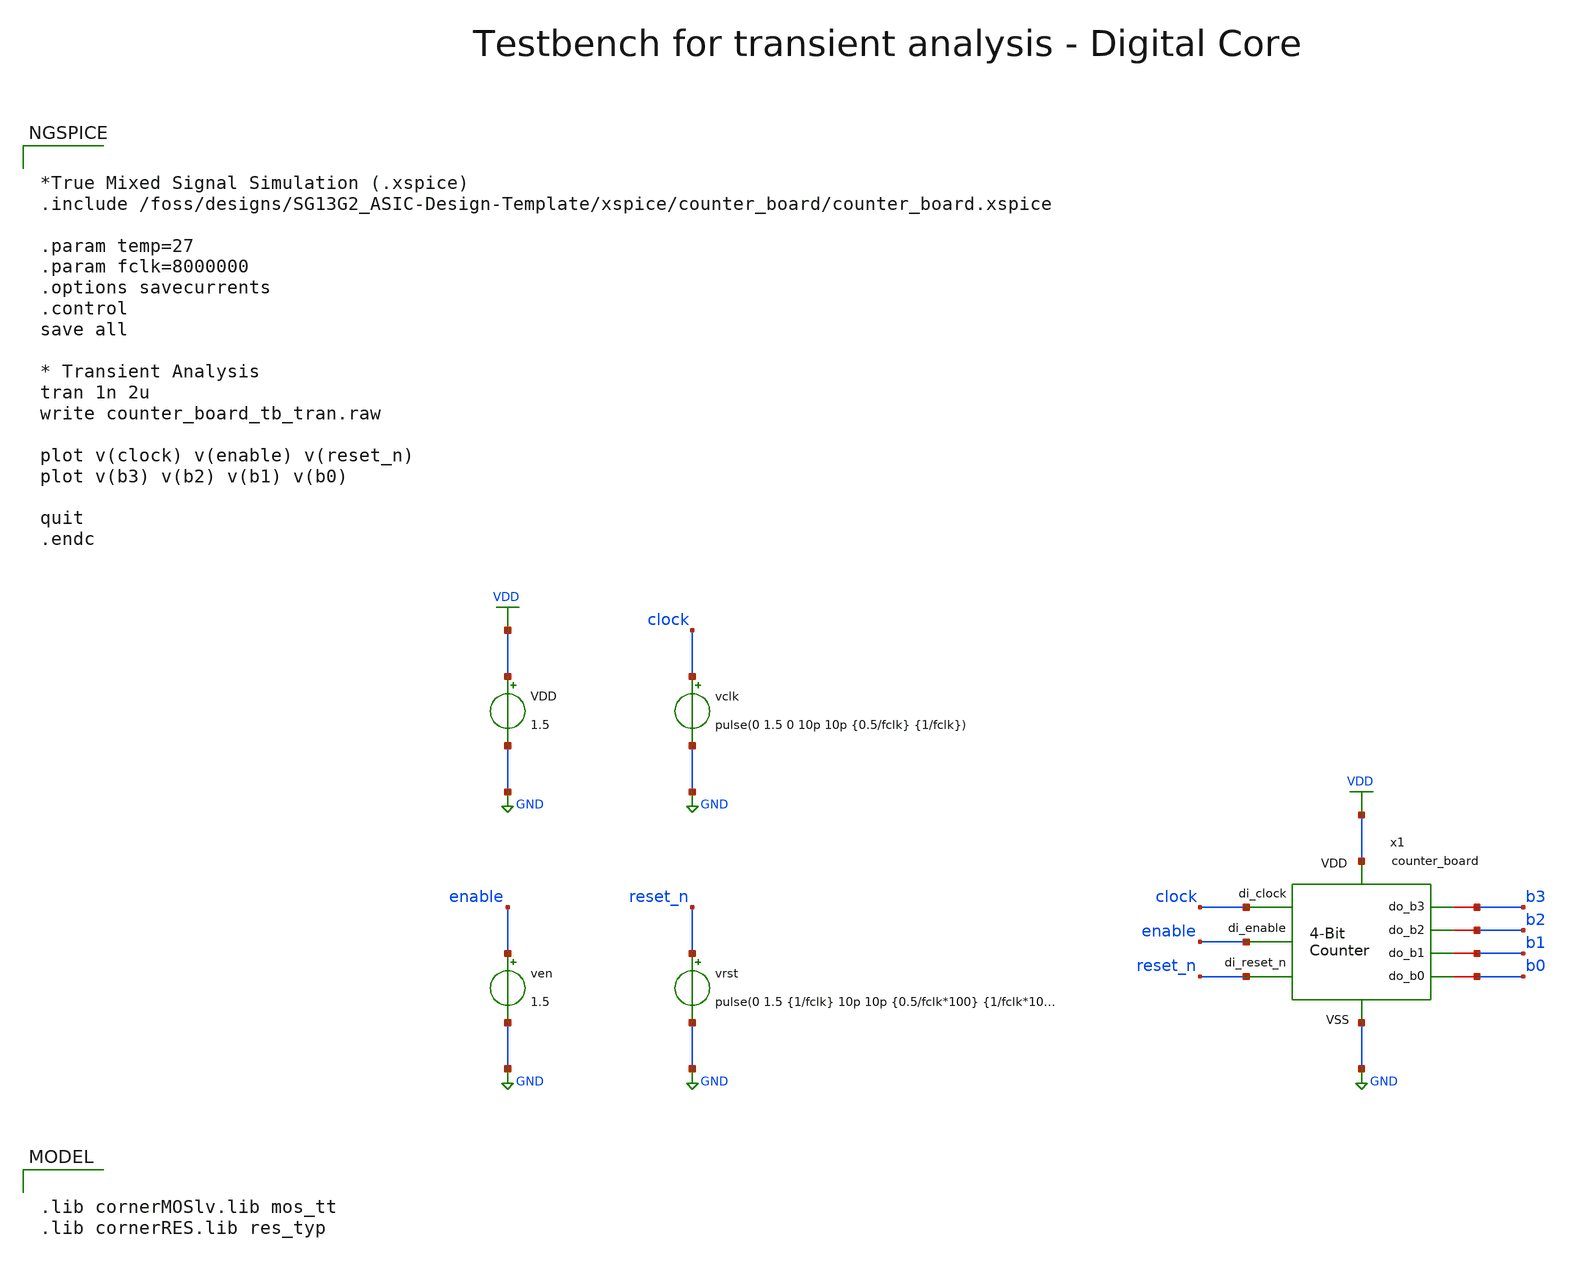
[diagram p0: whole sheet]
** sch_path: xschem/counter_board/testbenches/counter_board_tb_tran.sch
**.subckt counter_board_tb_tran
VDD VDD GND 1.5
vclk clock GND pulse(0 1.5 0 10p 10p {0.5/fclk} {1/fclk})
vrst reset_n GND pulse(0 1.5 {1/fclk} 10p 10p {0.5/fclk*100} {1/fclk*100})
x1 VDD GND clock b0 b1 b2 b3 reset_n counter_board
ven enable GND 1.5
**** begin user architecture code


*True Mixed Signal Simulation (.xspice)
.include /foss/designs/SG13G2_ASIC-Design-Template/xspice/counter_board/counter_board.xspice

.param temp=27
.param fclk=8000000
.options savecurrents
.control
save all

* Transient Analysis
tran 1n 2u
write counter_board_tb_tran.raw

plot v(clock) v(enable) v(reset_n)
plot v(b3) v(b2) v(b1) v(b0)

quit
.endc


.lib cornerMOSlv.lib mos_tt
.lib cornerRES.lib res_typ

**** end user architecture code
**.ends
.GLOBAL GND
.GLOBAL VDD
.end
